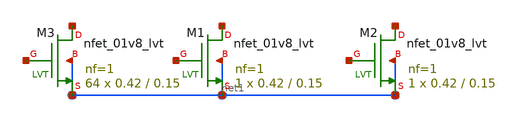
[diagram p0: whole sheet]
** sch_path: design/xschem/420x150_lvt_flat.sch
**.subckt 420x150_lvt_flat
XM2 net2 net3 net1 net1 sky130_fd_pr__nfet_01v8_lvt L=0.15 W=0.42 nf=1 ad='int((nf+1)/2) * W/nf * 0.29'
+ as='int((nf+2)/2) * W/nf * 0.29' pd='2*int((nf+1)/2) * (W/nf + 0.29)' ps='2*int((nf+2)/2) * (W/nf + 0.29)'
+ nrd='0.29 / W' nrs='0.29 / W' sa=0 sb=0 sd=0 mult=1 m=1
XM1 net4 net5 net1 net1 sky130_fd_pr__nfet_01v8_lvt L=0.15 W=0.42 nf=1 ad='int((nf+1)/2) * W/nf * 0.29'
+ as='int((nf+2)/2) * W/nf * 0.29' pd='2*int((nf+1)/2) * (W/nf + 0.29)' ps='2*int((nf+2)/2) * (W/nf + 0.29)'
+ nrd='0.29 / W' nrs='0.29 / W' sa=0 sb=0 sd=0 mult=1 m=1
XM3 net6 net7 net1 net1 sky130_fd_pr__nfet_01v8_lvt L=0.15 W=0.42 nf=1 ad='int((nf+1)/2) * W/nf * 0.29'
+ as='int((nf+2)/2) * W/nf * 0.29' pd='2*int((nf+1)/2) * (W/nf + 0.29)' ps='2*int((nf+2)/2) * (W/nf + 0.29)'
+ nrd='0.29 / W' nrs='0.29 / W' sa=0 sb=0 sd=0 mult=64 m=64
**.ends
.end
